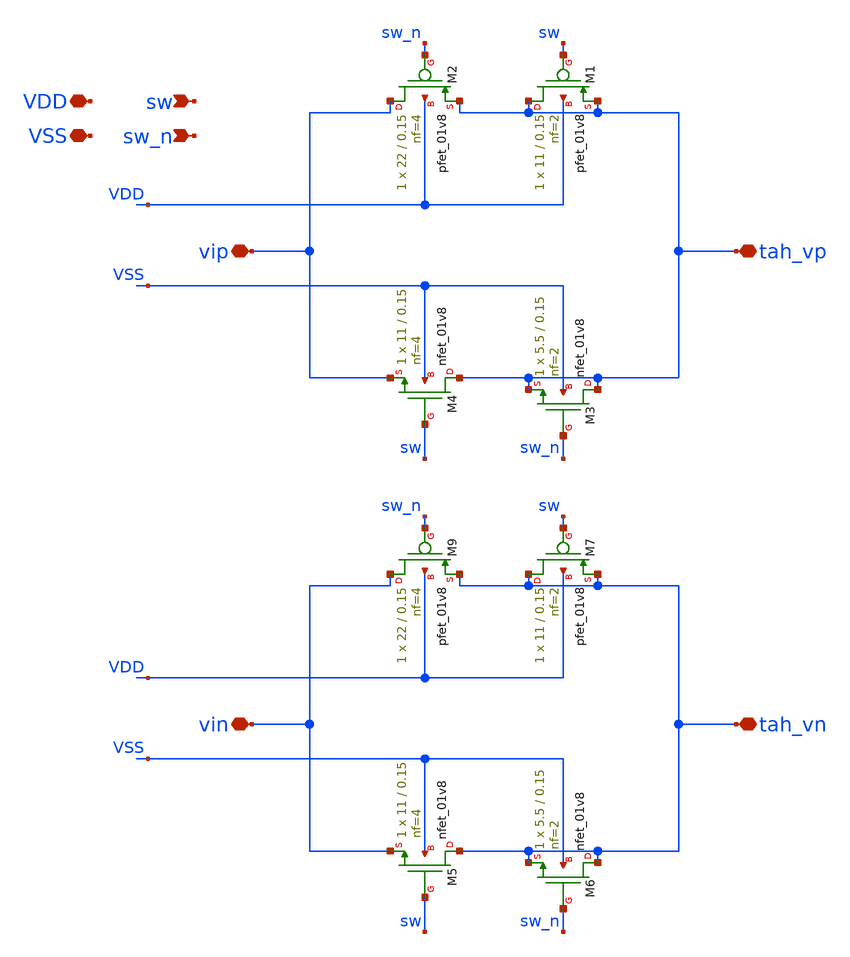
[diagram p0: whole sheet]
** sch_path: xschem/hgu_tah.sch
**.subckt hgu_tah tah_vp vip VDD VSS sw sw_n tah_vn vin
*.iopin tah_vp
*.iopin vip
*.iopin VDD
*.iopin VSS
*.ipin sw
*.ipin sw_n
*.iopin tah_vn
*.iopin vin
XM1 tah_vp sw tah_vp VDD sky130_fd_pr__pfet_01v8 L=0.15 W=11 nf=2 ad='int((nf+1)/2) * W/nf * 0.29' as='int((nf+2)/2) * W/nf * 0.29'
+ pd='2*int((nf+1)/2) * (W/nf + 0.29)' ps='2*int((nf+2)/2) * (W/nf + 0.29)' nrd='0.29 / W' nrs='0.29 / W'
+ sa=0 sb=0 sd=0 mult=1 m=1
XM4 tah_vp sw vip VSS sky130_fd_pr__nfet_01v8 L=0.15 W=11 nf=4 ad='int((nf+1)/2) * W/nf * 0.29' as='int((nf+2)/2) * W/nf * 0.29'
+ pd='2*int((nf+1)/2) * (W/nf + 0.29)' ps='2*int((nf+2)/2) * (W/nf + 0.29)' nrd='0.29 / W' nrs='0.29 / W'
+ sa=0 sb=0 sd=0 mult=1 m=1
XM2 vip sw_n tah_vp VDD sky130_fd_pr__pfet_01v8 L=0.15 W=22 nf=4 ad='int((nf+1)/2) * W/nf * 0.29' as='int((nf+2)/2) * W/nf * 0.29'
+ pd='2*int((nf+1)/2) * (W/nf + 0.29)' ps='2*int((nf+2)/2) * (W/nf + 0.29)' nrd='0.29 / W' nrs='0.29 / W'
+ sa=0 sb=0 sd=0 mult=1 m=1
XM3 tah_vp sw_n tah_vp VSS sky130_fd_pr__nfet_01v8 L=0.15 W=5.5 nf=2 ad='int((nf+1)/2) * W/nf * 0.29'
+ as='int((nf+2)/2) * W/nf * 0.29' pd='2*int((nf+1)/2) * (W/nf + 0.29)' ps='2*int((nf+2)/2) * (W/nf + 0.29)'
+ nrd='0.29 / W' nrs='0.29 / W' sa=0 sb=0 sd=0 mult=1 m=1
XM9 vin sw_n tah_vn VDD sky130_fd_pr__pfet_01v8 L=0.15 W=22 nf=4 ad='int((nf+1)/2) * W/nf * 0.29' as='int((nf+2)/2) * W/nf * 0.29'
+ pd='2*int((nf+1)/2) * (W/nf + 0.29)' ps='2*int((nf+2)/2) * (W/nf + 0.29)' nrd='0.29 / W' nrs='0.29 / W'
+ sa=0 sb=0 sd=0 mult=1 m=1
XM7 tah_vn sw tah_vn VDD sky130_fd_pr__pfet_01v8 L=0.15 W=11 nf=2 ad='int((nf+1)/2) * W/nf * 0.29' as='int((nf+2)/2) * W/nf * 0.29'
+ pd='2*int((nf+1)/2) * (W/nf + 0.29)' ps='2*int((nf+2)/2) * (W/nf + 0.29)' nrd='0.29 / W' nrs='0.29 / W'
+ sa=0 sb=0 sd=0 mult=1 m=1
XM5 tah_vn sw vin VSS sky130_fd_pr__nfet_01v8 L=0.15 W=11 nf=4 ad='int((nf+1)/2) * W/nf * 0.29' as='int((nf+2)/2) * W/nf * 0.29'
+ pd='2*int((nf+1)/2) * (W/nf + 0.29)' ps='2*int((nf+2)/2) * (W/nf + 0.29)' nrd='0.29 / W' nrs='0.29 / W'
+ sa=0 sb=0 sd=0 mult=1 m=1
XM6 tah_vn sw_n tah_vn VSS sky130_fd_pr__nfet_01v8 L=0.15 W=5.5 nf=2 ad='int((nf+1)/2) * W/nf * 0.29'
+ as='int((nf+2)/2) * W/nf * 0.29' pd='2*int((nf+1)/2) * (W/nf + 0.29)' ps='2*int((nf+2)/2) * (W/nf + 0.29)'
+ nrd='0.29 / W' nrs='0.29 / W' sa=0 sb=0 sd=0 mult=1 m=1
**.ends
.end
